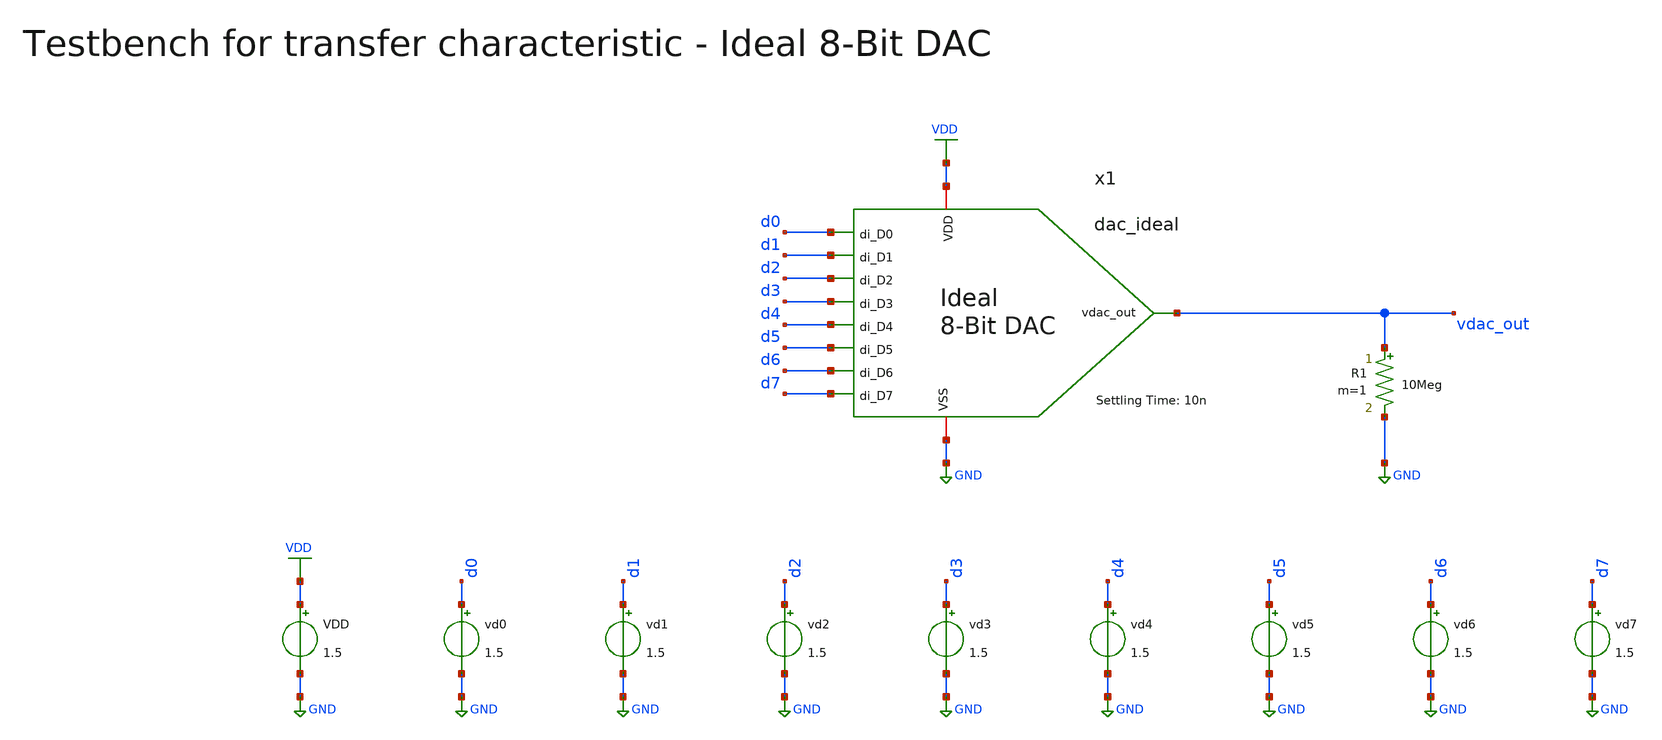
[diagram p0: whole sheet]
** sch_path: SG13G2_ATBS-ADC-main/xschem/dac/ideal/testbenches/dac_ideal_tb_tc.sch
**.subckt dac_ideal_tb_tc
VDD VDD GND 1.5
vd0 d0 GND 1.5
vd1 d1 GND 1.5
vd2 d2 GND 1.5
vd3 d3 GND 1.5
vd4 d4 GND 1.5
vd5 d5 GND 1.5
vd6 d6 GND 1.5
vd7 d7 GND 1.5
R1 vdac_out GND 10Meg m=1
x1 VDD d1 d4 d0 d2 d3 d7 d5 d6 vdac_out GND dac_ideal tsettle=10n
**** begin user architecture code


.param temp=27
.control
  set wr_vecnames
  set wr_singlescale
  let code = 0
  while code < 256
    if code eq 0
      let d0 = 0
    else
      let d0 = code % 2 * v(VDD)
    end
    if floor(code / 2) eq 0
      let d1 = 0
    else
      let d1 = floor(code / 2) % 2 * v(VDD)
    end
    if floor(code / 4) eq 0
      let d2 = 0
    else
      let d2 = floor(code / 4) % 2 * v(VDD)
    end
    if floor(code / 8) eq 0
      let d3 = 0
    else
      let d3 = floor(code / 8) % 2 * v(VDD)
    end
    if floor(code / 16) eq 0
      let d4 = 0
    else
      let d4 = floor(code / 16) % 2 * v(VDD)
    end
    if floor(code / 32) eq 0
      let d5 = 0
    else
      let d5 = floor(code / 32) % 2 * v(VDD)
    end
    if floor(code / 64) eq 0
      let d6 = 0
    else
      let d6 = floor(code / 64) % 2 * v(VDD)
    end
    if floor(code / 128) eq 0
      let d7 = 0
    else
      let d7 = floor(code / 128) % 2 * v(VDD)
    end
    alter vd0 $&d0
    alter vd1 $&d1
    alter vd2 $&d2
    alter vd3 $&d3
    alter vd4 $&d4
    alter vd5 $&d5
    alter vd6 $&d6
    alter vd7 $&d7
    save all
    op
    wrdata /foss/designs/SG13G2_ATBS-ADC-main/python/plot_simulations/data/dac_ideal_tb_tc.txt v(d0)
+ v(d1) v(d2) v(d3) v(d4) v(d5) v(d6) v(d7) v(vdac_out)
    if code eq 0
      set appendwrite
      set wr_vecnames = FALSE
    end
    let code = code + 1
  end
  quit
.endc


.lib cornerMOSlv.lib mos_tt
.lib cornerRES.lib res_typ

**** end user architecture code
**.ends

* expanding   symbol:  dac/ideal/dac_ideal.sym # of pins=11
** sym_path: SG13G2_ATBS-ADC-main/xschem/dac/ideal/dac_ideal.sym
** sch_path: SG13G2_ATBS-ADC-main/xschem/dac/ideal/dac_ideal.sch
.subckt dac_ideal VDD di_D1 di_D4 di_D0 di_D2 di_D3 di_D7 di_D5 di_D6 vdac_out VSS  tsettle=10n
*.opin vdac_out
*.ipin di_D0
*.iopin VSS
*.iopin VDD
*.ipin di_D1
*.ipin di_D2
*.ipin di_D3
*.ipin di_D4
*.ipin di_D5
*.ipin di_D6
*.ipin di_D7
R1 net1 VSS 3925 m=1
G1 VDD net1 di_D0 VSS 1u
G2 VDD net1 di_D1 VSS 2u
G3 VDD net1 di_D2 VSS 4u
G4 VDD net1 di_D3 VSS 8u
G5 VDD net1 di_D4 VSS 16u
G6 VDD net1 di_D5 VSS 32u
G7 VDD net1 di_D6 VSS 64u
G8 VDD net1 di_D7 VSS 128u
A1 net1 vdac_out VSS del_subckt
.model del_subckt delay(delay=tsettle buffer_size=8192)
.ends

.GLOBAL GND
.GLOBAL VDD
.end
